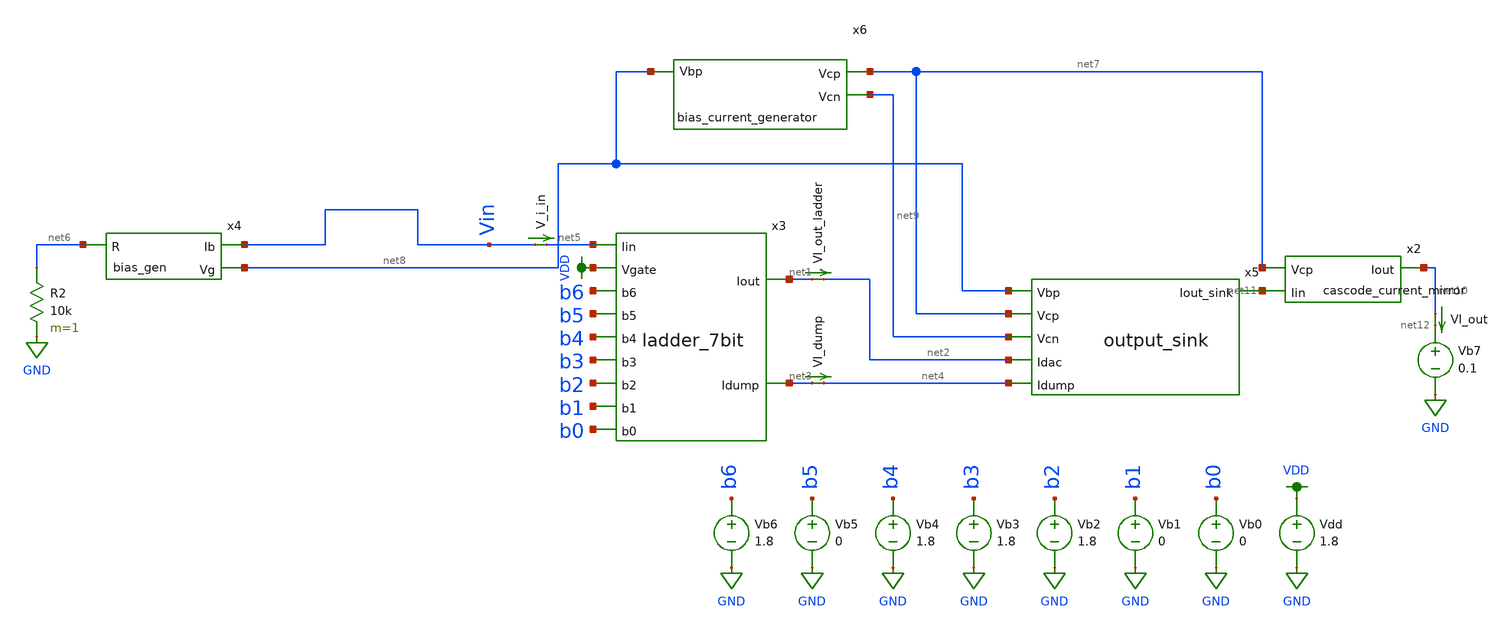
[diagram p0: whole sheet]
** sch_path: testing/test_harness_mc.sch
**.subckt test_harness_mc
x3 VDD net5 net3 net1 b5 b4 b1 b2 b3 b0 b6 ladder_7bit
VI_out_ladder net1 net2 0
.save i(vi_out_ladder)
VI_dump net3 net4 0
.save i(vi_dump)
V_i_in Vin net5 0
.save i(v_i_in)
x4 Vin net8 net6 bias_gen
R2 net6 GND 10k m=1
x5 net8 net7 net11 net9 net2 net4 output_sink
x6 net7 net8 net9 bias_current_generator
Vb0 b0 GND 0
Vb1 b1 GND 0
Vb2 b2 GND 1.8
Vb3 b3 GND 1.8
Vb4 b4 GND 1.8
Vb5 b5 GND 0
Vb6 b6 GND 1.8
Vdd VDD GND 1.8
Vb7 net12 GND 0.1
VI_out net10 net12 0
.save i(vi_out)
x2 net11 net10 net7 cascode_current_mirror
**** begin user architecture code

.option wnflag=1
.param MC_SWITCH=1.0
.lib ~/skywater/skywater-pdk/libraries/sky130_fd_pr_ngspice/latest/models/sky130.lib.spice tt


.control
  let runs = 10
  let run = 1
  while run <= runs
    set appendwrite = FALSE
    set wr_vecnames
    let code = 0
    while code < 128
      if code eq 0
        let b0 = 0
      else
        let b0 = code % 2
      end
      if floor(code / 2) eq 0
        let b1 = 0
      else
        let b1 = floor(code / 2) % 2
      end
      if floor(code / 4) eq 0
        let b2 = 0
      else
        let b2 = floor(code / 4) % 2
      end
      if floor(code / 8) eq 0
        let b3 = 0
      else
        let b3 = floor(code / 8) % 2
      end
      if floor(code / 16) eq 0
        let b4 = 0
      else
        let b4 = floor(code / 16) % 2
      end
      if floor(code / 32) eq 0
        let b5 = 0
      else
        let b5 = floor(code / 32) % 2
      end
      if floor(code / 64) eq 0
        let b6 = 0
      else
        let b6 = floor(code / 64) % 2
      end
      alter vb0 1.8*$&b0
      alter vb1 1.8*$&b1
      alter vb2 1.8*$&b2
      alter vb3 1.8*$&b3
      alter vb4 1.8*$&b4
      alter vb5 1.8*$&b5
      alter vb6 1.8*$&b6
      save all
      op
      wrdata ~/Documents/R2R-DAC/simulation/mc/mcdac{$&run}.txt i(V_i_in) i(VI_out) v(Vin)
      if code eq 0
        set appendwrite
        set wr_vecnames = FALSE
      end
      let code = code + 1
    end
    reset
    let run = run + 1
  end
.endc

**** end user architecture code
**.ends

* expanding   symbol:  ../modules/ladder_7bit.sym # of pins=11
** sym_path: testing/ladder_7bit.sym
** sch_path: testing/ladder_7bit.sch
.subckt ladder_7bit Vgate Iin Idump Iout b5 b4 b1 b2 b3 b0 b6
*.opin Idump
*.opin Iout
*.ipin Vgate
*.ipin Iin
*.ipin b6
*.ipin b5
*.ipin b4
*.ipin b3
*.ipin b2
*.ipin b1
*.ipin b0
x1 Iin net8 Vgate Idump Iout net1 b6 ladder_1bit
x2 net8 net9 Vgate Idump Iout net2 b5 ladder_1bit
x3 net9 net10 Vgate Idump Iout net3 b4 ladder_1bit
x4 net10 net11 Vgate Idump Iout net4 b3 ladder_1bit
x5 net11 net12 Vgate Idump Iout net5 b2 ladder_1bit
x6 net12 net13 Vgate Idump Iout net6 b1 ladder_1bit
x7 net13 net14 Vgate Idump Iout net7 b0 ladder_1bit
XM1 Idump Vgate net14 GND sky130_fd_pr__nfet_01v8 L=0.15 W=1 nf=1 ad='int((nf+1)/2) * W/nf * 0.29' as='int((nf+2)/2) * W/nf * 0.29'
+ pd='2*int((nf+1)/2) * (W/nf + 0.29)' ps='2*int((nf+2)/2) * (W/nf + 0.29)' nrd='0.29 / W' nrs='0.29 / W'
+ sa=0 sb=0 sd=0 mult=1 m=1
X8 b6 net15 VDD GND inverter
X9 b5 net16 VDD GND inverter
X10 b4 net17 VDD GND inverter
X11 b3 net18 VDD GND inverter
X12 b2 net19 VDD GND inverter
X13 b1 net20 VDD GND inverter
X14 b0 net21 VDD GND inverter
.ends


* expanding   symbol:  ../modules/bias_gen.sym # of pins=3
** sym_path: testing/bias_gen.sym
** sch_path: testing/bias_gen.sch
.subckt bias_gen Ib Vg R
*.ipin R
*.opin Ib
*.opin Vg
XM2 R net2 net2 GND sky130_fd_pr__nfet_01v8 L=4 W=96 nf=1 ad='int((nf+1)/2) * W/nf * 0.29' as='int((nf+2)/2) * W/nf * 0.29'
+ pd='2*int((nf+1)/2) * (W/nf + 0.29)' ps='2*int((nf+2)/2) * (W/nf + 0.29)' nrd='0.29 / W' nrs='0.29 / W'
+ sa=0 sb=0 sd=0 mult=1 m=1
XM3 VDD net1 net1 VDD sky130_fd_pr__pfet_01v8 L=4 W=12 nf=1 ad='int((nf+1)/2) * W/nf * 0.29' as='int((nf+2)/2) * W/nf * 0.29'
+ pd='2*int((nf+1)/2) * (W/nf + 0.29)' ps='2*int((nf+2)/2) * (W/nf + 0.29)' nrd='0.29 / W' nrs='0.29 / W'
+ sa=0 sb=0 sd=0 mult=1 m=1
XM1 VDD Vg net2 VDD sky130_fd_pr__pfet_01v8 L=4 W=12 nf=1 ad='int((nf+1)/2) * W/nf * 0.29' as='int((nf+2)/2) * W/nf * 0.29'
+ pd='2*int((nf+1)/2) * (W/nf + 0.29)' ps='2*int((nf+2)/2) * (W/nf + 0.29)' nrd='0.29 / W' nrs='0.29 / W'
+ sa=0 sb=0 sd=0 mult=1 m=1
XM4 Vg net1 VDD VDD sky130_fd_pr__pfet_01v8 L=4 W=12 nf=1 ad='int((nf+1)/2) * W/nf * 0.29' as='int((nf+2)/2) * W/nf * 0.29'
+ pd='2*int((nf+1)/2) * (W/nf + 0.29)' ps='2*int((nf+2)/2) * (W/nf + 0.29)' nrd='0.29 / W' nrs='0.29 / W'
+ sa=0 sb=0 sd=0 mult=1 m=1
XM5 net3 Vg VDD VDD sky130_fd_pr__pfet_01v8 L=4 W=12 nf=1 ad='int((nf+1)/2) * W/nf * 0.29' as='int((nf+2)/2) * W/nf * 0.29'
+ pd='2*int((nf+1)/2) * (W/nf + 0.29)' ps='2*int((nf+2)/2) * (W/nf + 0.29)' nrd='0.29 / W' nrs='0.29 / W'
+ sa=0 sb=0 sd=0 mult=1 m=1
XM7 Ib Vg VDD VDD sky130_fd_pr__pfet_01v8 L=4 W=12 nf=1 ad='int((nf+1)/2) * W/nf * 0.29' as='int((nf+2)/2) * W/nf * 0.29'
+ pd='2*int((nf+1)/2) * (W/nf + 0.29)' ps='2*int((nf+2)/2) * (W/nf + 0.29)' nrd='0.29 / W' nrs='0.29 / W'
+ sa=0 sb=0 sd=0 mult=1 m=1
XM6 net1 net2 GND GND sky130_fd_pr__nfet_01v8 L=4 W=12 nf=1 ad='int((nf+1)/2) * W/nf * 0.29' as='int((nf+2)/2) * W/nf * 0.29'
+ pd='2*int((nf+1)/2) * (W/nf + 0.29)' ps='2*int((nf+2)/2) * (W/nf + 0.29)' nrd='0.29 / W' nrs='0.29 / W'
+ sa=0 sb=0 sd=0 mult=1 m=1
XM8 GND net3 Vg GND sky130_fd_pr__nfet_01v8 L=4 W=12 nf=1 ad='int((nf+1)/2) * W/nf * 0.29' as='int((nf+2)/2) * W/nf * 0.29'
+ pd='2*int((nf+1)/2) * (W/nf + 0.29)' ps='2*int((nf+2)/2) * (W/nf + 0.29)' nrd='0.29 / W' nrs='0.29 / W'
+ sa=0 sb=0 sd=0 mult=1 m=1
XM9 net3 net3 GND GND sky130_fd_pr__nfet_01v8 L=4 W=12 nf=1 ad='int((nf+1)/2) * W/nf * 0.29' as='int((nf+2)/2) * W/nf * 0.29'
+ pd='2*int((nf+1)/2) * (W/nf + 0.29)' ps='2*int((nf+2)/2) * (W/nf + 0.29)' nrd='0.29 / W' nrs='0.29 / W'
+ sa=0 sb=0 sd=0 mult=1 m=1
.ends


* expanding   symbol:  ../modules/output_sink.sym # of pins=6
** sym_path: testing/output_sink.sym
** sch_path: testing/output_sink.sch
.subckt output_sink Vbp Vcp Iout_sink Vcn Idac Idump
*.ipin Idump
*.ipin Idac
*.ipin Vcn
*.ipin Vcp
*.ipin Vbp
*.opin Iout_sink
XM1 net1 Vcn Idump GND sky130_fd_pr__nfet_01v8 L=0.5 W=12 nf=1 ad='int((nf+1)/2) * W/nf * 0.29' as='int((nf+2)/2) * W/nf * 0.29'
+ pd='2*int((nf+1)/2) * (W/nf + 0.29)' ps='2*int((nf+2)/2) * (W/nf + 0.29)' nrd='0.29 / W' nrs='0.29 / W'
+ sa=0 sb=0 sd=0 mult=1 m=1
XM8 net4 Vbp VDD VDD sky130_fd_pr__pfet_01v8 L=0.5 W=12 nf=1 ad='int((nf+1)/2) * W/nf * 0.29' as='int((nf+2)/2) * W/nf * 0.29'
+ pd='2*int((nf+1)/2) * (W/nf + 0.29)' ps='2*int((nf+2)/2) * (W/nf + 0.29)' nrd='0.29 / W' nrs='0.29 / W'
+ sa=0 sb=0 sd=0 mult=1 m=1
XM7 net5 Vbp VDD VDD sky130_fd_pr__pfet_01v8 L=0.5 W=12 nf=1 ad='int((nf+1)/2) * W/nf * 0.29' as='int((nf+2)/2) * W/nf * 0.29'
+ pd='2*int((nf+1)/2) * (W/nf + 0.29)' ps='2*int((nf+2)/2) * (W/nf + 0.29)' nrd='0.29 / W' nrs='0.29 / W'
+ sa=0 sb=0 sd=0 mult=1 m=1
XM9 net6 Vbp VDD VDD sky130_fd_pr__pfet_01v8 L=0.5 W=12 nf=1 ad='int((nf+1)/2) * W/nf * 0.29' as='int((nf+2)/2) * W/nf * 0.29'
+ pd='2*int((nf+1)/2) * (W/nf + 0.29)' ps='2*int((nf+2)/2) * (W/nf + 0.29)' nrd='0.29 / W' nrs='0.29 / W'
+ sa=0 sb=0 sd=0 mult=1 m=1
XM10 Iout_sink Vcp net6 VDD sky130_fd_pr__pfet_01v8 L=0.5 W=12 nf=1 ad='int((nf+1)/2) * W/nf * 0.29'
+ as='int((nf+2)/2) * W/nf * 0.29' pd='2*int((nf+1)/2) * (W/nf + 0.29)' ps='2*int((nf+2)/2) * (W/nf + 0.29)'
+ nrd='0.29 / W' nrs='0.29 / W' sa=0 sb=0 sd=0 mult=1 m=1
XM11 net2 Vcp net5 VDD sky130_fd_pr__pfet_01v8 L=0.5 W=12 nf=1 ad='int((nf+1)/2) * W/nf * 0.29' as='int((nf+2)/2) * W/nf * 0.29'
+ pd='2*int((nf+1)/2) * (W/nf + 0.29)' ps='2*int((nf+2)/2) * (W/nf + 0.29)' nrd='0.29 / W' nrs='0.29 / W'
+ sa=0 sb=0 sd=0 mult=1 m=1
XM12 net1 Vcp net4 VDD sky130_fd_pr__pfet_01v8 L=0.5 W=12 nf=1 ad='int((nf+1)/2) * W/nf * 0.29' as='int((nf+2)/2) * W/nf * 0.29'
+ pd='2*int((nf+1)/2) * (W/nf + 0.29)' ps='2*int((nf+2)/2) * (W/nf + 0.29)' nrd='0.29 / W' nrs='0.29 / W'
+ sa=0 sb=0 sd=0 mult=1 m=1
XM3 net2 Vcn Idac GND sky130_fd_pr__nfet_01v8 L=0.5 W=12 nf=1 ad='int((nf+1)/2) * W/nf * 0.29' as='int((nf+2)/2) * W/nf * 0.29'
+ pd='2*int((nf+1)/2) * (W/nf + 0.29)' ps='2*int((nf+2)/2) * (W/nf + 0.29)' nrd='0.29 / W' nrs='0.29 / W'
+ sa=0 sb=0 sd=0 mult=1 m=1
XM5 Iout_sink Vcn net3 GND sky130_fd_pr__nfet_01v8 L=0.5 W=12 nf=1 ad='int((nf+1)/2) * W/nf * 0.29' as='int((nf+2)/2) * W/nf * 0.29'
+ pd='2*int((nf+1)/2) * (W/nf + 0.29)' ps='2*int((nf+2)/2) * (W/nf + 0.29)' nrd='0.29 / W' nrs='0.29 / W'
+ sa=0 sb=0 sd=0 mult=1 m=1
XM6 net3 net2 GND GND sky130_fd_pr__nfet_01v8 L=0.5 W=12 nf=1 ad='int((nf+1)/2) * W/nf * 0.29' as='int((nf+2)/2) * W/nf * 0.29'
+ pd='2*int((nf+1)/2) * (W/nf + 0.29)' ps='2*int((nf+2)/2) * (W/nf + 0.29)' nrd='0.29 / W' nrs='0.29 / W'
+ sa=0 sb=0 sd=0 mult=1 m=1
XM13 Idac net2 GND GND sky130_fd_pr__nfet_01v8 L=0.5 W=12 nf=1 ad='int((nf+1)/2) * W/nf * 0.29' as='int((nf+2)/2) * W/nf * 0.29'
+ pd='2*int((nf+1)/2) * (W/nf + 0.29)' ps='2*int((nf+2)/2) * (W/nf + 0.29)' nrd='0.29 / W' nrs='0.29 / W'
+ sa=0 sb=0 sd=0 mult=1 m=1
XM14 Idump net1 GND GND sky130_fd_pr__nfet_01v8 L=0.5 W=12 nf=1 ad='int((nf+1)/2) * W/nf * 0.29' as='int((nf+2)/2) * W/nf * 0.29'
+ pd='2*int((nf+1)/2) * (W/nf + 0.29)' ps='2*int((nf+2)/2) * (W/nf + 0.29)' nrd='0.29 / W' nrs='0.29 / W'
+ sa=0 sb=0 sd=0 mult=1 m=1
.ends


* expanding   symbol:  ../modules/bias_current_generator.sym # of pins=3
** sym_path: testing/bias_current_generator.sym
** sch_path: testing/bias_current_generator.sch
.subckt bias_current_generator Vcp Vbp Vcn
*.opin Vcn
*.opin Vcp
*.ipin Vbp
XM4 Vcn Vbp VDD VDD sky130_fd_pr__pfet_01v8 L=0.5 W=12 nf=1 ad='int((nf+1)/2) * W/nf * 0.29' as='int((nf+2)/2) * W/nf * 0.29'
+ pd='2*int((nf+1)/2) * (W/nf + 0.29)' ps='2*int((nf+2)/2) * (W/nf + 0.29)' nrd='0.29 / W' nrs='0.29 / W'
+ sa=0 sb=0 sd=0 mult=1 m=1
XM11 Vcn Vcn net2 GND sky130_fd_pr__nfet_01v8 L=0.5 W=12 nf=1 ad='int((nf+1)/2) * W/nf * 0.29' as='int((nf+2)/2) * W/nf * 0.29'
+ pd='2*int((nf+1)/2) * (W/nf + 0.29)' ps='2*int((nf+2)/2) * (W/nf + 0.29)' nrd='0.29 / W' nrs='0.29 / W'
+ sa=0 sb=0 sd=0 mult=1 m=1
XM8 net5 net5 net2 GND sky130_fd_pr__nfet_01v8 L=0.5 W=12 nf=1 ad='int((nf+1)/2) * W/nf * 0.29' as='int((nf+2)/2) * W/nf * 0.29'
+ pd='2*int((nf+1)/2) * (W/nf + 0.29)' ps='2*int((nf+2)/2) * (W/nf + 0.29)' nrd='0.29 / W' nrs='0.29 / W'
+ sa=0 sb=0 sd=0 mult=1 m=1
XM9 net2 net5 net5 GND sky130_fd_pr__nfet_01v8 L=0.5 W=12 nf=1 ad='int((nf+1)/2) * W/nf * 0.29' as='int((nf+2)/2) * W/nf * 0.29'
+ pd='2*int((nf+1)/2) * (W/nf + 0.29)' ps='2*int((nf+2)/2) * (W/nf + 0.29)' nrd='0.29 / W' nrs='0.29 / W'
+ sa=0 sb=0 sd=0 mult=1 m=1
XM10 net5 net5 net2 GND sky130_fd_pr__nfet_01v8 L=0.5 W=12 nf=1 ad='int((nf+1)/2) * W/nf * 0.29' as='int((nf+2)/2) * W/nf * 0.29'
+ pd='2*int((nf+1)/2) * (W/nf + 0.29)' ps='2*int((nf+2)/2) * (W/nf + 0.29)' nrd='0.29 / W' nrs='0.29 / W'
+ sa=0 sb=0 sd=0 mult=1 m=1
XM22 net2 net5 net5 GND sky130_fd_pr__nfet_01v8 L=0.5 W=12 nf=1 ad='int((nf+1)/2) * W/nf * 0.29' as='int((nf+2)/2) * W/nf * 0.29'
+ pd='2*int((nf+1)/2) * (W/nf + 0.29)' ps='2*int((nf+2)/2) * (W/nf + 0.29)' nrd='0.29 / W' nrs='0.29 / W'
+ sa=0 sb=0 sd=0 mult=1 m=1
XM23 GND net5 net2 GND sky130_fd_pr__nfet_01v8 L=0.5 W=12 nf=1 ad='int((nf+1)/2) * W/nf * 0.29' as='int((nf+2)/2) * W/nf * 0.29'
+ pd='2*int((nf+1)/2) * (W/nf + 0.29)' ps='2*int((nf+2)/2) * (W/nf + 0.29)' nrd='0.29 / W' nrs='0.29 / W'
+ sa=0 sb=0 sd=0 mult=1 m=1
XM28 Vcp net1 GND GND sky130_fd_pr__nfet_01v8 L=0.5 W=12 nf=1 ad='int((nf+1)/2) * W/nf * 0.29' as='int((nf+2)/2) * W/nf * 0.29'
+ pd='2*int((nf+1)/2) * (W/nf + 0.29)' ps='2*int((nf+2)/2) * (W/nf + 0.29)' nrd='0.29 / W' nrs='0.29 / W'
+ sa=0 sb=0 sd=0 mult=1 m=1
XM12 GND net1 net7 GND sky130_fd_pr__nfet_01v8 L=0.5 W=12 nf=1 ad='int((nf+1)/2) * W/nf * 0.29' as='int((nf+2)/2) * W/nf * 0.29'
+ pd='2*int((nf+1)/2) * (W/nf + 0.29)' ps='2*int((nf+2)/2) * (W/nf + 0.29)' nrd='0.29 / W' nrs='0.29 / W'
+ sa=0 sb=0 sd=0 mult=1 m=1
XM13 net7 net1 net8 GND sky130_fd_pr__nfet_01v8 L=0.5 W=12 nf=1 ad='int((nf+1)/2) * W/nf * 0.29' as='int((nf+2)/2) * W/nf * 0.29'
+ pd='2*int((nf+1)/2) * (W/nf + 0.29)' ps='2*int((nf+2)/2) * (W/nf + 0.29)' nrd='0.29 / W' nrs='0.29 / W'
+ sa=0 sb=0 sd=0 mult=1 m=1
XM14 net8 net1 net13 GND sky130_fd_pr__nfet_01v8 L=0.5 W=12 nf=1 ad='int((nf+1)/2) * W/nf * 0.29' as='int((nf+2)/2) * W/nf * 0.29'
+ pd='2*int((nf+1)/2) * (W/nf + 0.29)' ps='2*int((nf+2)/2) * (W/nf + 0.29)' nrd='0.29 / W' nrs='0.29 / W'
+ sa=0 sb=0 sd=0 mult=1 m=1
XM15 net13 net1 net12 GND sky130_fd_pr__nfet_01v8 L=0.5 W=12 nf=1 ad='int((nf+1)/2) * W/nf * 0.29' as='int((nf+2)/2) * W/nf * 0.29'
+ pd='2*int((nf+1)/2) * (W/nf + 0.29)' ps='2*int((nf+2)/2) * (W/nf + 0.29)' nrd='0.29 / W' nrs='0.29 / W'
+ sa=0 sb=0 sd=0 mult=1 m=1
XM24 net12 net1 net10 GND sky130_fd_pr__nfet_01v8 L=0.5 W=12 nf=1 ad='int((nf+1)/2) * W/nf * 0.29' as='int((nf+2)/2) * W/nf * 0.29'
+ pd='2*int((nf+1)/2) * (W/nf + 0.29)' ps='2*int((nf+2)/2) * (W/nf + 0.29)' nrd='0.29 / W' nrs='0.29 / W'
+ sa=0 sb=0 sd=0 mult=1 m=1
XM5 VDD Vbp net3 VDD sky130_fd_pr__pfet_01v8 L=0.5 W=12 nf=1 ad='int((nf+1)/2) * W/nf * 0.29' as='int((nf+2)/2) * W/nf * 0.29'
+ pd='2*int((nf+1)/2) * (W/nf + 0.29)' ps='2*int((nf+2)/2) * (W/nf + 0.29)' nrd='0.29 / W' nrs='0.29 / W'
+ sa=0 sb=0 sd=0 mult=1 m=1
XM6 net3 Vbp net4 VDD sky130_fd_pr__pfet_01v8 L=0.5 W=12 nf=1 ad='int((nf+1)/2) * W/nf * 0.29' as='int((nf+2)/2) * W/nf * 0.29'
+ pd='2*int((nf+1)/2) * (W/nf + 0.29)' ps='2*int((nf+2)/2) * (W/nf + 0.29)' nrd='0.29 / W' nrs='0.29 / W'
+ sa=0 sb=0 sd=0 mult=1 m=1
XM7 net4 Vbp net6 VDD sky130_fd_pr__pfet_01v8 L=0.5 W=12 nf=1 ad='int((nf+1)/2) * W/nf * 0.29' as='int((nf+2)/2) * W/nf * 0.29'
+ pd='2*int((nf+1)/2) * (W/nf + 0.29)' ps='2*int((nf+2)/2) * (W/nf + 0.29)' nrd='0.29 / W' nrs='0.29 / W'
+ sa=0 sb=0 sd=0 mult=1 m=1
XM20 net6 Vbp net11 VDD sky130_fd_pr__pfet_01v8 L=0.5 W=12 nf=1 ad='int((nf+1)/2) * W/nf * 0.29' as='int((nf+2)/2) * W/nf * 0.29'
+ pd='2*int((nf+1)/2) * (W/nf + 0.29)' ps='2*int((nf+2)/2) * (W/nf + 0.29)' nrd='0.29 / W' nrs='0.29 / W'
+ sa=0 sb=0 sd=0 mult=1 m=1
XM21 net11 Vbp net5 VDD sky130_fd_pr__pfet_01v8 L=0.5 W=12 nf=1 ad='int((nf+1)/2) * W/nf * 0.29' as='int((nf+2)/2) * W/nf * 0.29'
+ pd='2*int((nf+1)/2) * (W/nf + 0.29)' ps='2*int((nf+2)/2) * (W/nf + 0.29)' nrd='0.29 / W' nrs='0.29 / W'
+ sa=0 sb=0 sd=0 mult=1 m=1
XM16 Vcp Vcp net9 VDD sky130_fd_pr__pfet_01v8 L=0.5 W=12 nf=1 ad='int((nf+1)/2) * W/nf * 0.29' as='int((nf+2)/2) * W/nf * 0.29'
+ pd='2*int((nf+1)/2) * (W/nf + 0.29)' ps='2*int((nf+2)/2) * (W/nf + 0.29)' nrd='0.29 / W' nrs='0.29 / W'
+ sa=0 sb=0 sd=0 mult=1 m=1
XM17 net10 net10 net9 VDD sky130_fd_pr__pfet_01v8 L=0.5 W=12 nf=1 ad='int((nf+1)/2) * W/nf * 0.29' as='int((nf+2)/2) * W/nf * 0.29'
+ pd='2*int((nf+1)/2) * (W/nf + 0.29)' ps='2*int((nf+2)/2) * (W/nf + 0.29)' nrd='0.29 / W' nrs='0.29 / W'
+ sa=0 sb=0 sd=0 mult=1 m=1
XM18 net9 net10 net10 VDD sky130_fd_pr__pfet_01v8 L=0.5 W=12 nf=1 ad='int((nf+1)/2) * W/nf * 0.29' as='int((nf+2)/2) * W/nf * 0.29'
+ pd='2*int((nf+1)/2) * (W/nf + 0.29)' ps='2*int((nf+2)/2) * (W/nf + 0.29)' nrd='0.29 / W' nrs='0.29 / W'
+ sa=0 sb=0 sd=0 mult=1 m=1
XM19 net10 net10 net9 VDD sky130_fd_pr__pfet_01v8 L=0.5 W=12 nf=1 ad='int((nf+1)/2) * W/nf * 0.29' as='int((nf+2)/2) * W/nf * 0.29'
+ pd='2*int((nf+1)/2) * (W/nf + 0.29)' ps='2*int((nf+2)/2) * (W/nf + 0.29)' nrd='0.29 / W' nrs='0.29 / W'
+ sa=0 sb=0 sd=0 mult=1 m=1
XM25 net9 net10 net10 VDD sky130_fd_pr__pfet_01v8 L=0.5 W=12 nf=1 ad='int((nf+1)/2) * W/nf * 0.29' as='int((nf+2)/2) * W/nf * 0.29'
+ pd='2*int((nf+1)/2) * (W/nf + 0.29)' ps='2*int((nf+2)/2) * (W/nf + 0.29)' nrd='0.29 / W' nrs='0.29 / W'
+ sa=0 sb=0 sd=0 mult=1 m=1
XM26 VDD net10 net9 VDD sky130_fd_pr__pfet_01v8 L=0.5 W=12 nf=1 ad='int((nf+1)/2) * W/nf * 0.29' as='int((nf+2)/2) * W/nf * 0.29'
+ pd='2*int((nf+1)/2) * (W/nf + 0.29)' ps='2*int((nf+2)/2) * (W/nf + 0.29)' nrd='0.29 / W' nrs='0.29 / W'
+ sa=0 sb=0 sd=0 mult=1 m=1
XM2 net1 Vbp VDD VDD sky130_fd_pr__pfet_01v8 L=0.5 W=12 nf=1 ad='int((nf+1)/2) * W/nf * 0.29' as='int((nf+2)/2) * W/nf * 0.29'
+ pd='2*int((nf+1)/2) * (W/nf + 0.29)' ps='2*int((nf+2)/2) * (W/nf + 0.29)' nrd='0.29 / W' nrs='0.29 / W'
+ sa=0 sb=0 sd=0 mult=1 m=1
XM3 net1 net1 GND GND sky130_fd_pr__nfet_01v8 L=0.5 W=12 nf=1 ad='int((nf+1)/2) * W/nf * 0.29' as='int((nf+2)/2) * W/nf * 0.29'
+ pd='2*int((nf+1)/2) * (W/nf + 0.29)' ps='2*int((nf+2)/2) * (W/nf + 0.29)' nrd='0.29 / W' nrs='0.29 / W'
+ sa=0 sb=0 sd=0 mult=1 m=1
.ends


* expanding   symbol:  /home/madvlsi/Documents/R2R-DAC/modules/cascode_current_mirror.sym # of
*+ pins=3
** sym_path: modules/cascode_current_mirror.sym
** sch_path: modules/cascode_current_mirror.sch
.subckt cascode_current_mirror Iin Iout Vcp
*.ipin Vcp
*.ipin Iin
*.opin Iout
XM5 net1 Iin VDD VDD sky130_fd_pr__pfet_01v8 L=8 W=24 nf=1 ad='int((nf+1)/2) * W/nf * 0.29' as='int((nf+2)/2) * W/nf * 0.29'
+ pd='2*int((nf+1)/2) * (W/nf + 0.29)' ps='2*int((nf+2)/2) * (W/nf + 0.29)' nrd='0.29 / W' nrs='0.29 / W'
+ sa=0 sb=0 sd=0 mult=1 m=1
XM1 Iin Vcp net1 VDD sky130_fd_pr__pfet_01v8 L=8 W=24 nf=1 ad='int((nf+1)/2) * W/nf * 0.29' as='int((nf+2)/2) * W/nf * 0.29'
+ pd='2*int((nf+1)/2) * (W/nf + 0.29)' ps='2*int((nf+2)/2) * (W/nf + 0.29)' nrd='0.29 / W' nrs='0.29 / W'
+ sa=0 sb=0 sd=0 mult=1 m=1
XM2 net2 Iin VDD VDD sky130_fd_pr__pfet_01v8 L=8 W=24 nf=1 ad='int((nf+1)/2) * W/nf * 0.29' as='int((nf+2)/2) * W/nf * 0.29'
+ pd='2*int((nf+1)/2) * (W/nf + 0.29)' ps='2*int((nf+2)/2) * (W/nf + 0.29)' nrd='0.29 / W' nrs='0.29 / W'
+ sa=0 sb=0 sd=0 mult=1 m=1
XM3 Iout Vcp net2 VDD sky130_fd_pr__pfet_01v8 L=8 W=24 nf=1 ad='int((nf+1)/2) * W/nf * 0.29' as='int((nf+2)/2) * W/nf * 0.29'
+ pd='2*int((nf+1)/2) * (W/nf + 0.29)' ps='2*int((nf+2)/2) * (W/nf + 0.29)' nrd='0.29 / W' nrs='0.29 / W'
+ sa=0 sb=0 sd=0 mult=1 m=1
.ends


* expanding   symbol:  /home/madvlsi/R2R-DAC/ladder_1bit.sym # of pins=7
** sym_path: testing/ladder_1bit.sym
** sch_path: testing/ladder_1bit.sch
.subckt ladder_1bit Iin_in Iin_out Vg I_dump Iout B_bar B
*.ipin Iin_in
*.ipin Vg
*.ipin B
*.ipin B_bar
*.opin Iin_out
*.opin I_dump
*.opin Iout
XM5 net1 Vg Iin_in GND sky130_fd_pr__nfet_01v8 L=0.15 W=1 nf=1 ad='int((nf+1)/2) * W/nf * 0.29' as='int((nf+2)/2) * W/nf * 0.29'
+ pd='2*int((nf+1)/2) * (W/nf + 0.29)' ps='2*int((nf+2)/2) * (W/nf + 0.29)' nrd='0.29 / W' nrs='0.29 / W'
+ sa=0 sb=0 sd=0 mult=1 m=1
XM6 Iout B net1 GND sky130_fd_pr__nfet_01v8 L=0.15 W=1 nf=1 ad='int((nf+1)/2) * W/nf * 0.29' as='int((nf+2)/2) * W/nf * 0.29'
+ pd='2*int((nf+1)/2) * (W/nf + 0.29)' ps='2*int((nf+2)/2) * (W/nf + 0.29)' nrd='0.29 / W' nrs='0.29 / W'
+ sa=0 sb=0 sd=0 mult=1 m=1
XM7 net1 B_bar I_dump GND sky130_fd_pr__nfet_01v8 L=0.15 W=1 nf=1 ad='int((nf+1)/2) * W/nf * 0.29' as='int((nf+2)/2) * W/nf * 0.29'
+ pd='2*int((nf+1)/2) * (W/nf + 0.29)' ps='2*int((nf+2)/2) * (W/nf + 0.29)' nrd='0.29 / W' nrs='0.29 / W'
+ sa=0 sb=0 sd=0 mult=1 m=1
XM8 Iin_in Vg Iin_out GND sky130_fd_pr__nfet_01v8 L=0.15 W=1 nf=1 ad='int((nf+1)/2) * W/nf * 0.29' as='int((nf+2)/2) * W/nf * 0.29'
+ pd='2*int((nf+1)/2) * (W/nf + 0.29)' ps='2*int((nf+2)/2) * (W/nf + 0.29)' nrd='0.29 / W' nrs='0.29 / W'
+ sa=0 sb=0 sd=0 mult=1 m=1
.ends


* expanding   symbol:  /home/madvlsi/Documents/mp1/inverter.sym # of pins=4
** sym_path: /home/madvlsi/Documents/mp1/inverter.sym
** sch_path: /home/madvlsi/Documents/mp1/inverter.sch
.subckt inverter A Y VP VN
*.ipin A
*.iopin VP
*.iopin VN
*.opin Y
XM3 Y A VP VP sky130_fd_pr__pfet_01v8 L=0.15 W=1 nf=1 ad='int((nf+1)/2) * W/nf * 0.29' as='int((nf+2)/2) * W/nf * 0.29'
+ pd='2*int((nf+1)/2) * (W/nf + 0.29)' ps='2*int((nf+2)/2) * (W/nf + 0.29)' nrd='0.29 / W' nrs='0.29 / W'
+ sa=0 sb=0 sd=0 mult=1 m=1
XM4 Y A VN VN sky130_fd_pr__nfet_01v8 L=0.15 W=1 nf=1 ad='int((nf+1)/2) * W/nf * 0.29' as='int((nf+2)/2) * W/nf * 0.29'
+ pd='2*int((nf+1)/2) * (W/nf + 0.29)' ps='2*int((nf+2)/2) * (W/nf + 0.29)' nrd='0.29 / W' nrs='0.29 / W'
+ sa=0 sb=0 sd=0 mult=1 m=1
.ends

.GLOBAL VDD
.GLOBAL GND
.end
